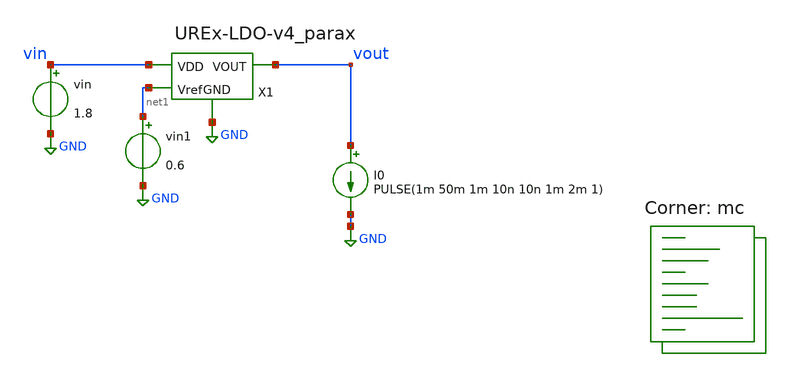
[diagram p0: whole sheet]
** sch_path: xschem/corner-sims/LoadReg-v4-cornersim.sch
**.subckt LoadReg-v4-cornersim
vin vin GND 1.8
X1 vin vout GND net1 UREx-LDO-v4_parax
I0 vout GND PULSE(1m 50m 1m 10n 10n 1m 2m 1)
vin1 net1 GND 0.6
**** begin user architecture code


.param mc_mm_switch=1
.param mc_pr_switch=1
.param Rload=20
.control
  tran 1u 3m
  wrdata loadreg.csv v(vout)

  set appendwrite

  repeat 100
    reset
    tran 1u 3m
    wrdata loadreg.csv v(vout)
  end
.endc


.lib $::SKYWATER_MODELS/sky130.lib.spice mc
**** end user architecture code
**.ends

* expanding   symbol:  UREx-LDO-v4_parax.sym # of pins=4
** sym_path: xschem/UREx-LDO-v4.sym
.include [file normalize UREx-LDO-v4_parax.spice]
.GLOBAL GND
.end
